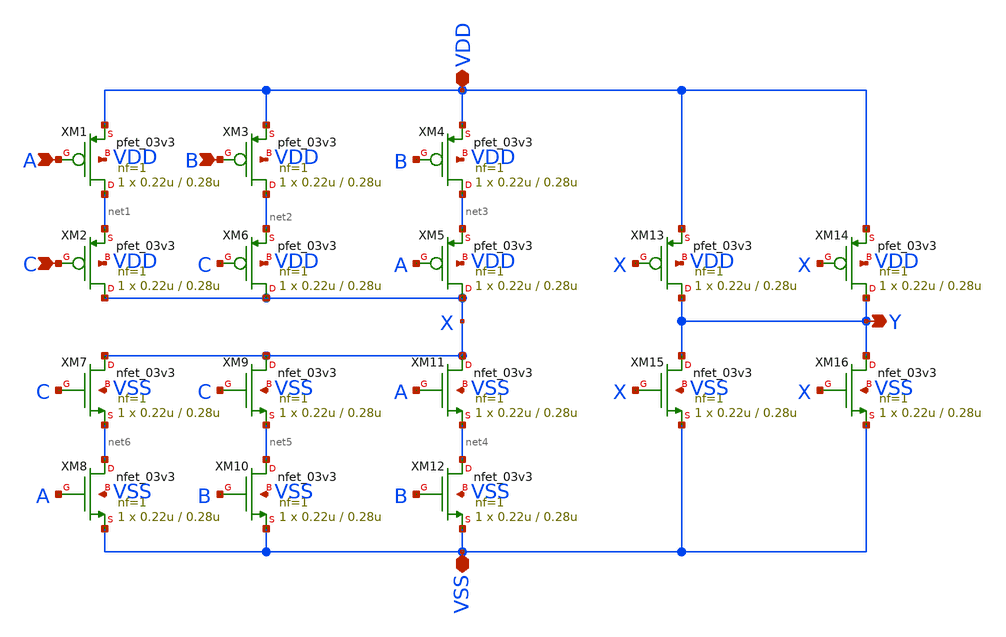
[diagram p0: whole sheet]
** sch_path: xschem/maj3.sch
**.subckt maj3 A C B Y VDD VSS
*.ipin A
*.ipin C
*.ipin B
*.opin Y
*.iopin VDD
*.iopin VSS
XM1 net1 A VDD VDD pfet_03v3 L=0.28u W=0.22u nf=1 ad='int((nf+1)/2) * W/nf * 0.18u' as='int((nf+2)/2) * W/nf * 0.18u'
+ pd='2*int((nf+1)/2) * (W/nf + 0.18u)' ps='2*int((nf+2)/2) * (W/nf + 0.18u)' nrd='0.18u / W' nrs='0.18u / W'
+ sa=0 sb=0 sd=0 m=1
XM2 X C net1 VDD pfet_03v3 L=0.28u W=0.22u nf=1 ad='int((nf+1)/2) * W/nf * 0.18u' as='int((nf+2)/2) * W/nf * 0.18u'
+ pd='2*int((nf+1)/2) * (W/nf + 0.18u)' ps='2*int((nf+2)/2) * (W/nf + 0.18u)' nrd='0.18u / W' nrs='0.18u / W'
+ sa=0 sb=0 sd=0 m=1
XM3 net2 B VDD VDD pfet_03v3 L=0.28u W=0.22u nf=1 ad='int((nf+1)/2) * W/nf * 0.18u' as='int((nf+2)/2) * W/nf * 0.18u'
+ pd='2*int((nf+1)/2) * (W/nf + 0.18u)' ps='2*int((nf+2)/2) * (W/nf + 0.18u)' nrd='0.18u / W' nrs='0.18u / W'
+ sa=0 sb=0 sd=0 m=1
XM4 net3 B VDD VDD pfet_03v3 L=0.28u W=0.22u nf=1 ad='int((nf+1)/2) * W/nf * 0.18u' as='int((nf+2)/2) * W/nf * 0.18u'
+ pd='2*int((nf+1)/2) * (W/nf + 0.18u)' ps='2*int((nf+2)/2) * (W/nf + 0.18u)' nrd='0.18u / W' nrs='0.18u / W'
+ sa=0 sb=0 sd=0 m=1
XM5 X A net3 VDD pfet_03v3 L=0.28u W=0.22u nf=1 ad='int((nf+1)/2) * W/nf * 0.18u' as='int((nf+2)/2) * W/nf * 0.18u'
+ pd='2*int((nf+1)/2) * (W/nf + 0.18u)' ps='2*int((nf+2)/2) * (W/nf + 0.18u)' nrd='0.18u / W' nrs='0.18u / W'
+ sa=0 sb=0 sd=0 m=1
XM6 X C net2 VDD pfet_03v3 L=0.28u W=0.22u nf=1 ad='int((nf+1)/2) * W/nf * 0.18u' as='int((nf+2)/2) * W/nf * 0.18u'
+ pd='2*int((nf+1)/2) * (W/nf + 0.18u)' ps='2*int((nf+2)/2) * (W/nf + 0.18u)' nrd='0.18u / W' nrs='0.18u / W'
+ sa=0 sb=0 sd=0 m=1
XM7 X C net6 VSS nfet_03v3 L=0.28u W=0.22u nf=1 ad='int((nf+1)/2) * W/nf * 0.18u' as='int((nf+2)/2) * W/nf * 0.18u'
+ pd='2*int((nf+1)/2) * (W/nf + 0.18u)' ps='2*int((nf+2)/2) * (W/nf + 0.18u)' nrd='0.18u / W' nrs='0.18u / W'
+ sa=0 sb=0 sd=0 m=1
XM8 net6 A VSS VSS nfet_03v3 L=0.28u W=0.22u nf=1 ad='int((nf+1)/2) * W/nf * 0.18u' as='int((nf+2)/2) * W/nf * 0.18u'
+ pd='2*int((nf+1)/2) * (W/nf + 0.18u)' ps='2*int((nf+2)/2) * (W/nf + 0.18u)' nrd='0.18u / W' nrs='0.18u / W'
+ sa=0 sb=0 sd=0 m=1
XM9 X C net5 VSS nfet_03v3 L=0.28u W=0.22u nf=1 ad='int((nf+1)/2) * W/nf * 0.18u' as='int((nf+2)/2) * W/nf * 0.18u'
+ pd='2*int((nf+1)/2) * (W/nf + 0.18u)' ps='2*int((nf+2)/2) * (W/nf + 0.18u)' nrd='0.18u / W' nrs='0.18u / W'
+ sa=0 sb=0 sd=0 m=1
XM10 net5 B VSS VSS nfet_03v3 L=0.28u W=0.22u nf=1 ad='int((nf+1)/2) * W/nf * 0.18u' as='int((nf+2)/2) * W/nf * 0.18u'
+ pd='2*int((nf+1)/2) * (W/nf + 0.18u)' ps='2*int((nf+2)/2) * (W/nf + 0.18u)' nrd='0.18u / W' nrs='0.18u / W'
+ sa=0 sb=0 sd=0 m=1
XM11 X A net4 VSS nfet_03v3 L=0.28u W=0.22u nf=1 ad='int((nf+1)/2) * W/nf * 0.18u' as='int((nf+2)/2) * W/nf * 0.18u'
+ pd='2*int((nf+1)/2) * (W/nf + 0.18u)' ps='2*int((nf+2)/2) * (W/nf + 0.18u)' nrd='0.18u / W' nrs='0.18u / W'
+ sa=0 sb=0 sd=0 m=1
XM12 net4 B VSS VSS nfet_03v3 L=0.28u W=0.22u nf=1 ad='int((nf+1)/2) * W/nf * 0.18u' as='int((nf+2)/2) * W/nf * 0.18u'
+ pd='2*int((nf+1)/2) * (W/nf + 0.18u)' ps='2*int((nf+2)/2) * (W/nf + 0.18u)' nrd='0.18u / W' nrs='0.18u / W'
+ sa=0 sb=0 sd=0 m=1
XM13 Y X VDD VDD pfet_03v3 L=0.28u W=0.22u nf=1 ad='int((nf+1)/2) * W/nf * 0.18u' as='int((nf+2)/2) * W/nf * 0.18u'
+ pd='2*int((nf+1)/2) * (W/nf + 0.18u)' ps='2*int((nf+2)/2) * (W/nf + 0.18u)' nrd='0.18u / W' nrs='0.18u / W'
+ sa=0 sb=0 sd=0 m=1
XM14 Y X VDD VDD pfet_03v3 L=0.28u W=0.22u nf=1 ad='int((nf+1)/2) * W/nf * 0.18u' as='int((nf+2)/2) * W/nf * 0.18u'
+ pd='2*int((nf+1)/2) * (W/nf + 0.18u)' ps='2*int((nf+2)/2) * (W/nf + 0.18u)' nrd='0.18u / W' nrs='0.18u / W'
+ sa=0 sb=0 sd=0 m=1
XM15 Y X VSS VSS nfet_03v3 L=0.28u W=0.22u nf=1 ad='int((nf+1)/2) * W/nf * 0.18u' as='int((nf+2)/2) * W/nf * 0.18u'
+ pd='2*int((nf+1)/2) * (W/nf + 0.18u)' ps='2*int((nf+2)/2) * (W/nf + 0.18u)' nrd='0.18u / W' nrs='0.18u / W'
+ sa=0 sb=0 sd=0 m=1
XM16 Y X VSS VSS nfet_03v3 L=0.28u W=0.22u nf=1 ad='int((nf+1)/2) * W/nf * 0.18u' as='int((nf+2)/2) * W/nf * 0.18u'
+ pd='2*int((nf+1)/2) * (W/nf + 0.18u)' ps='2*int((nf+2)/2) * (W/nf + 0.18u)' nrd='0.18u / W' nrs='0.18u / W'
+ sa=0 sb=0 sd=0 m=1
**.ends
.end
